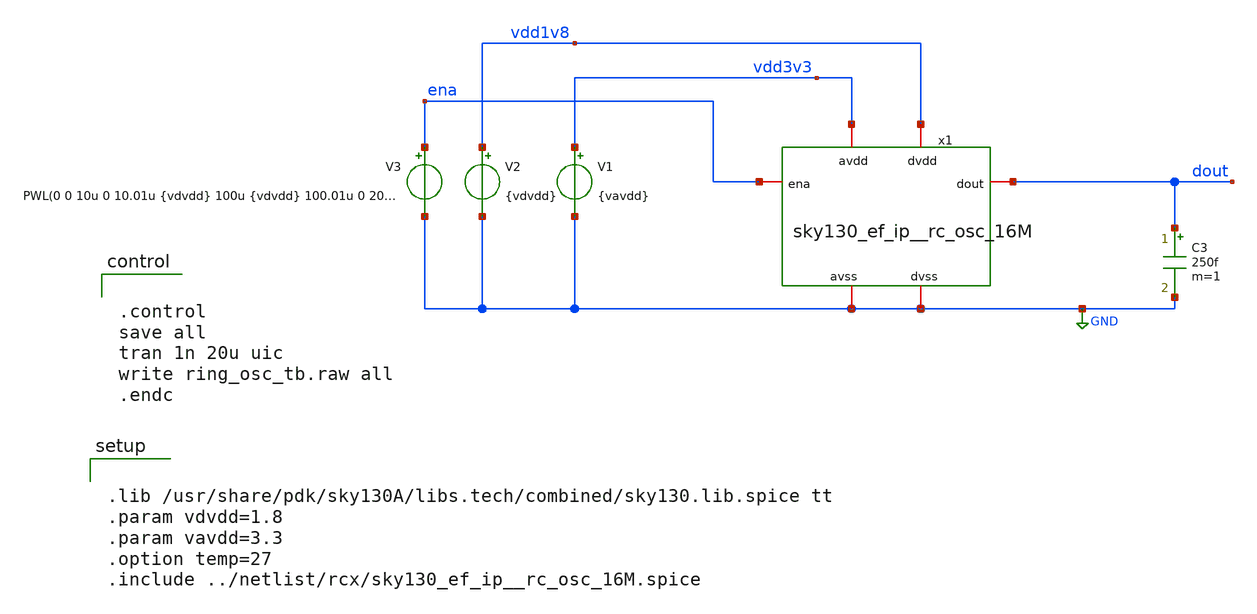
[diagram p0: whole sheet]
** sch_path: cace/ring_osc_tb.sch
**.subckt ring_osc_tb
x1 ena vdd1v8 vdd3v3 GND GND dout sky130_ef_ip__rc_osc_16M
V1 vdd3v3 GND {vavdd}
V2 vdd1v8 GND {vdvdd}
C3 dout GND 250f m=1
V3 ena GND PWL(0 0 10u 0 10.01u {vdvdd} 100u {vdvdd} 100.01u 0 200u 0 200.01u {vdvdd})
**** begin user architecture code


.control
save all
tran 1n 20u uic
write ring_osc_tb.raw all
.endc




.lib /usr/share/pdk/sky130A/libs.tech/combined/sky130.lib.spice tt
.param vdvdd=1.8
.param vavdd=3.3
.option temp=27
.include ../netlist/rcx/sky130_ef_ip__rc_osc_16M.spice


**** end user architecture code
**.ends
.GLOBAL GND
.end
